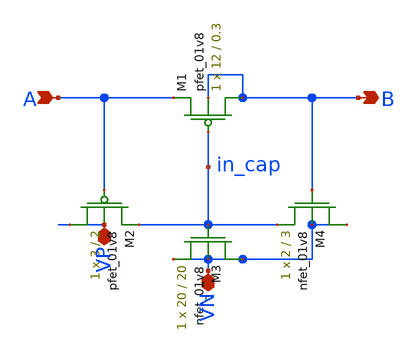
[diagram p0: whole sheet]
** sch_path: schematic/memristor_emulator.sch
**.subckt memristor_emulator A VN VP B
*.ipin A
*.iopin VN
*.iopin VP
*.opin B
XM1 B in_cap A B sky130_fd_pr__pfet_01v8 L=0.3 W=12 nf=1 ad='int((nf+1)/2) * W/nf * 0.29' as='int((nf+2)/2) * W/nf * 0.29'
+ pd='2*int((nf+1)/2) * (W/nf + 0.29)' ps='2*int((nf+2)/2) * (W/nf + 0.29)' nrd='0.29 / W' nrs='0.29 / W'
+ sa=0 sb=0 sd=0 mult=1 m=1
XM2 VP A in_cap VP sky130_fd_pr__pfet_01v8 L=2 W=3 nf=1 ad='int((nf+1)/2) * W/nf * 0.29' as='int((nf+2)/2) * W/nf * 0.29'
+ pd='2*int((nf+1)/2) * (W/nf + 0.29)' ps='2*int((nf+2)/2) * (W/nf + 0.29)' nrd='0.29 / W' nrs='0.29 / W'
+ sa=0 sb=0 sd=0 mult=1 m=1
XM3 VN in_cap VN VN sky130_fd_pr__nfet_01v8 L=20 W=20 nf=1 ad='int((nf+1)/2) * W/nf * 0.29' as='int((nf+2)/2) * W/nf * 0.29'
+ pd='2*int((nf+1)/2) * (W/nf + 0.29)' ps='2*int((nf+2)/2) * (W/nf + 0.29)' nrd='0.29 / W' nrs='0.29 / W'
+ sa=0 sb=0 sd=0 mult=1 m=1
XM4 VN B in_cap VN sky130_fd_pr__nfet_01v8 L=3 W=2 nf=1 ad='int((nf+1)/2) * W/nf * 0.29' as='int((nf+2)/2) * W/nf * 0.29'
+ pd='2*int((nf+1)/2) * (W/nf + 0.29)' ps='2*int((nf+2)/2) * (W/nf + 0.29)' nrd='0.29 / W' nrs='0.29 / W'
+ sa=0 sb=0 sd=0 mult=1 m=1
**.ends
.end
